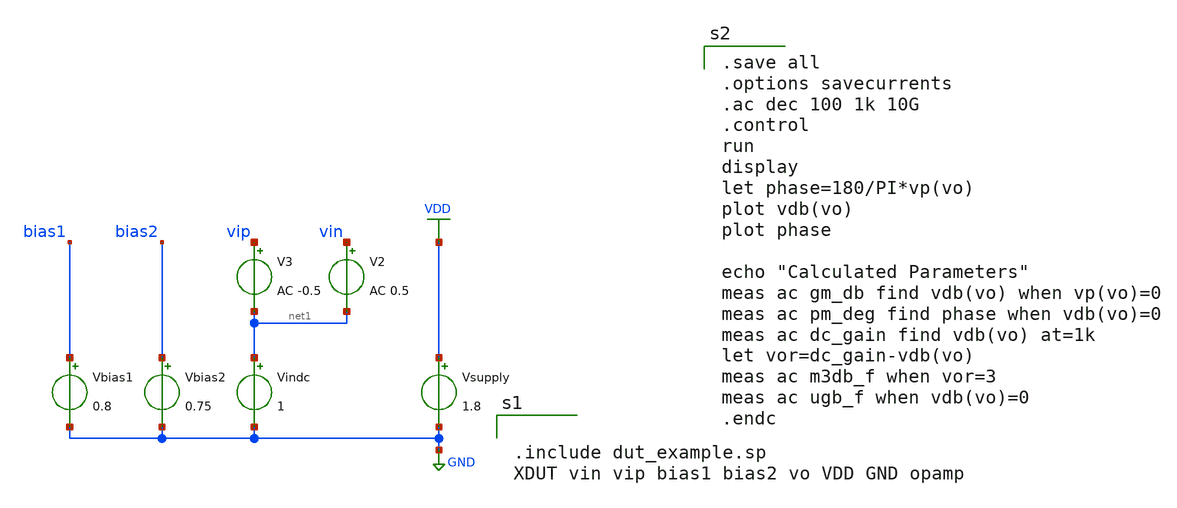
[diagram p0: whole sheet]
** sch_path: SKY130/opamp_perf_eval/04_cmrr.sch
**.subckt 04_cmrr
Vsupply VDD GND 1.8
V2 vin net1 AC 0.5
V3 vip net1 AC -0.5
Vbias2 bias2 GND 0.75
Vbias1 bias1 GND 0.8
Vindc net1 GND 1
**** begin user architecture code


.include dut_example.sp
XDUT vin vip bias1 bias2 vo VDD GND opamp


.lib $::SKYWATER_MODELS/sky130.lib.spice tt
.include $::PDKPATH/libs.ref/sky130_fd_sc_hvl/spice/sky130_fd_sc_hvl.spice

.save all
.options savecurrents
.ac dec 100 1k 10G
.control
run
display
let phase=180/PI*vp(vo)
plot vdb(vo)
plot phase

echo "Calculated Parameters"
meas ac gm_db find vdb(vo) when vp(vo)=0
meas ac pm_deg find phase when vdb(vo)=0
meas ac dc_gain find vdb(vo) at=1k
let vor=dc_gain-vdb(vo)
meas ac m3db_f when vor=3
meas ac ugb_f when vdb(vo)=0
.endc


**** end user architecture code
**.ends
.GLOBAL GND
.GLOBAL VDD
.end
